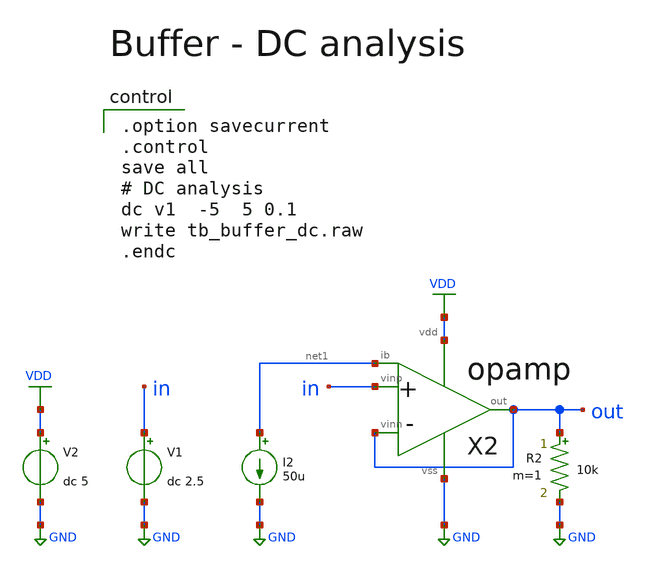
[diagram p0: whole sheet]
** sch_path: member_project/AM_Radio/Yamada3/xschem/tb_buffer_dc.sch
**.subckt tb_buffer_dc
V2 VDD GND dc 5
V1 in GND dc 2.5
I2 net1 GND 50u
R2 out GND 10k m=1
X2 in out net1 out VDD GND opamp
**** begin user architecture code

.option savecurrent
.control
save all
# DC analysis
dc v1  -5  5 0.1
write tb_buffer_dc.raw
.endc

 .include $::LIB/ip62_models
**** end user architecture code
**.ends
.GLOBAL GND
.GLOBAL VDD
.end
